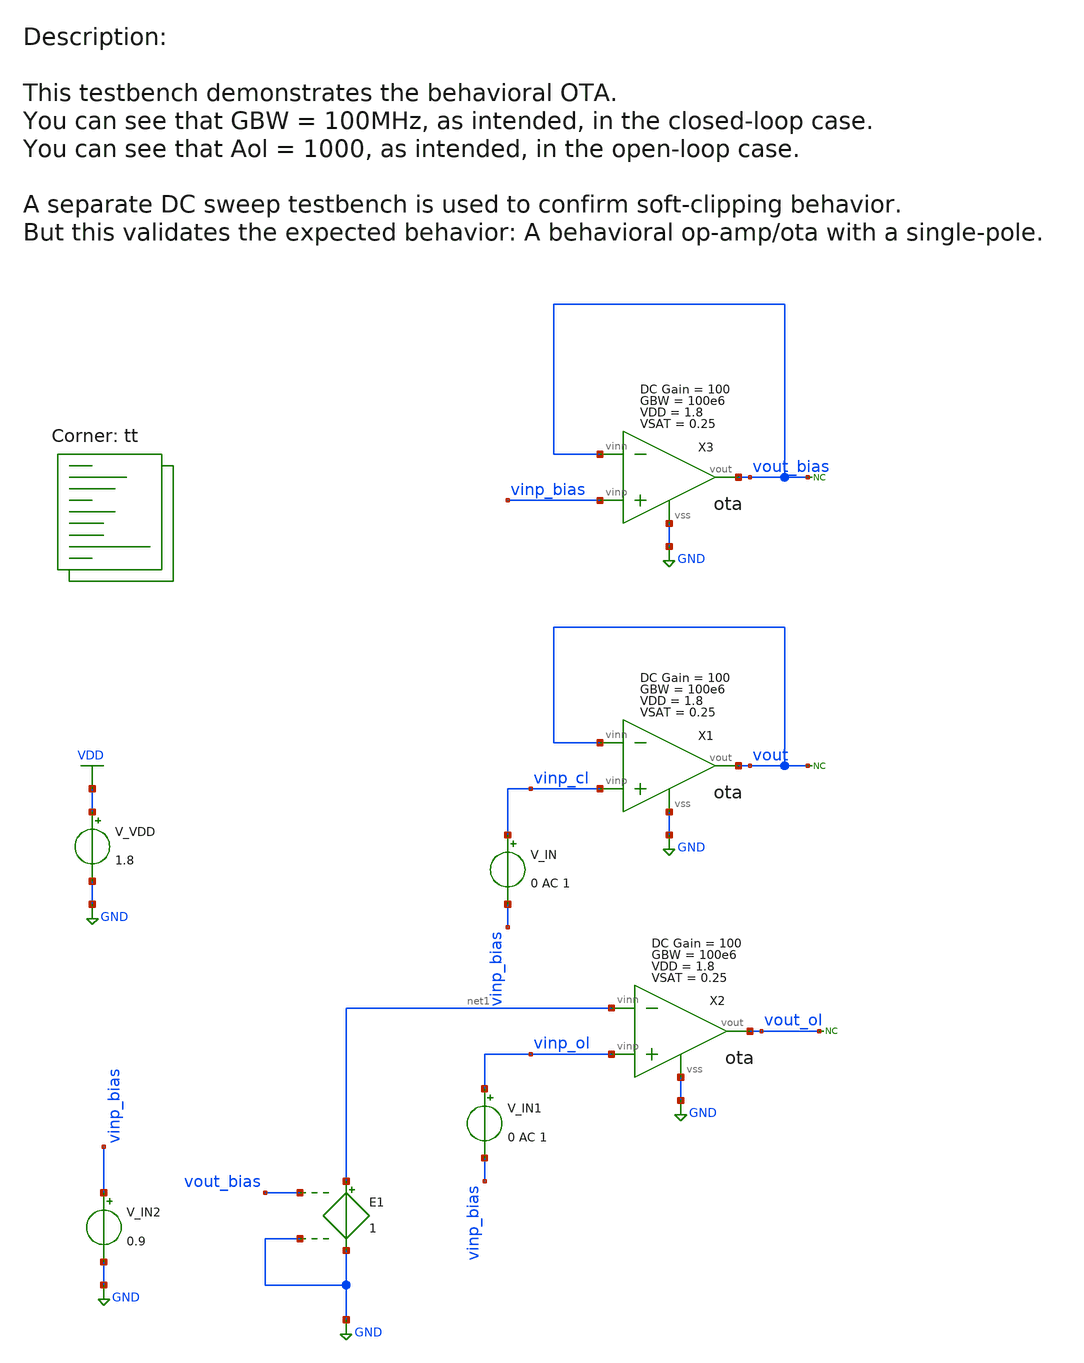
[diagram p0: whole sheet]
** sch_path: xsch/tb/tb_ota_1_AC_sweep.sch
**.subckt tb_ota_1_AC_sweep
V_VDD VDD GND 1.8
.save i(v_vdd)
V_IN vinp_cl vinp_bias 0 AC 1
.save i(v_in)
* noconn vout
X1 vinp_cl vout GND vout ota Ao=100 VDD=1.8 VSAT=0.25 GBW=100e6 Rout_ol=100
* noconn vout_ol
X2 vinp_ol vout_ol GND net1 ota Ao=100 VDD=1.8 VSAT=0.25 GBW=100e6 Rout_ol=100
V_IN1 vinp_ol vinp_bias 0 AC 1
.save i(v_in1)
* noconn vout_bias
X3 vinp_bias vout_bias GND vout_bias ota Ao=100 VDD=1.8 VSAT=0.25 GBW=100e6 Rout_ol=100
V_IN2 vinp_bias GND 0.9
.save i(v_in2)
E1 net1 GND vout_bias GND 1
**** begin user architecture code


.control
  save all
  ac dec 100 1 1e9
  plot db(v(vout))
  plot v(vout_ol)
  write tb_ota_1_AC_sweep.raw
.endc



.lib $::SKYWATER_MODELS/sky130.lib.spice tt
**** end user architecture code
**.ends

* expanding   symbol:  behavioral/ota.sym # of pins=4
** sym_path: xsch/behavioral/ota.sym
** sch_path: xsch/behavioral/ota.sch
.subckt ota vinp vout vss vinn  Ao=1000 VDD=1.8 VSAT=0.25 GBW=100e6 Rout_ol=100
*.ipin vinp
*.ipin vinn
*.opin vout
*.iopin vss
R1 vcvs1_out_filt vcvs1_out 10k m=1
C1 vcvs1_out_filt vss {Ao/2/3.14/GBW/10e3} m=1
Rout_ol vout vcvs2_out {Rout_ol} m=1
V1 vinp_int vinp 0
V2 vinn_int vinn 0
B2 vcvs1_out vss V = {VDD/2 + (VDD/2-VSAT)*(tanh(V(vinp_int, vinn_int)*Ao/(VDD/2-VSAT)))}
B1 vcvs2_out vss V = {V(vcvs1_out_filt, vss)*1}
.ends

.GLOBAL GND
.GLOBAL VDD
.end
